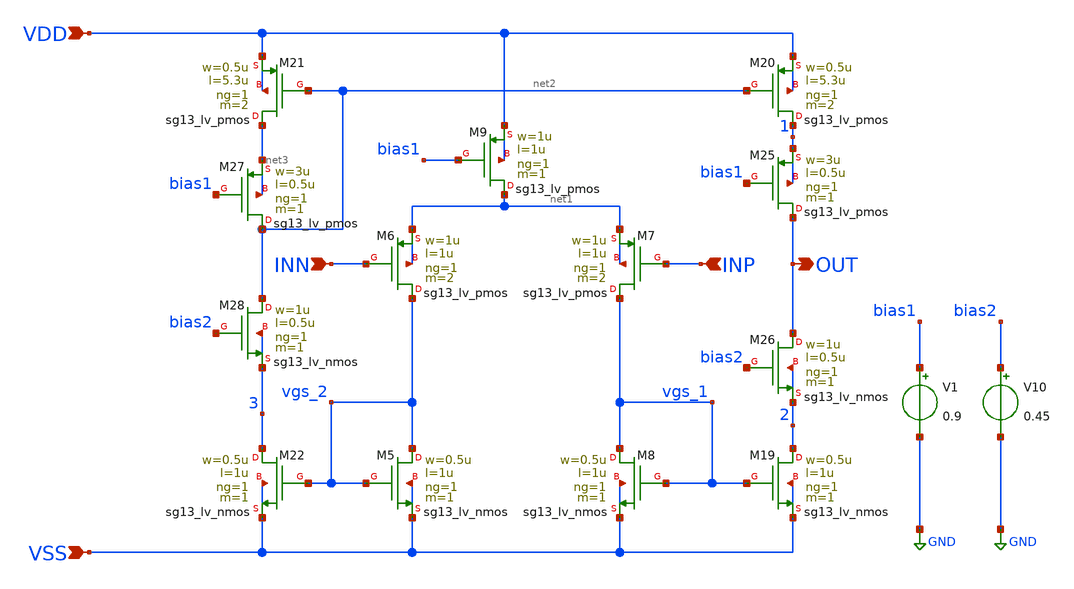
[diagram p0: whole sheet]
** sch_path: 10_xschem/ota.sch
**.subckt ota VDD VSS INN INP OUT
*.ipin VDD
*.ipin VSS
*.ipin INN
*.ipin INP
*.opin OUT
XM5 vgs_2 vgs_2 VSS VSS sg13_lv_nmos w=0.5u l=1u ng=1 m=1 mm_ok=1
XM6 vgs_2 INN net1 net1 sg13_lv_pmos w=1u l=1u ng=1 m=2 mm_ok=1
XM7 vgs_1 INP net1 net1 sg13_lv_pmos w=1u l=1u ng=1 m=2 mm_ok=1
XM8 vgs_1 vgs_1 VSS VSS sg13_lv_nmos w=0.5u l=1u ng=1 m=1 mm_ok=1
XM9 net1 bias1 VDD VDD sg13_lv_pmos w=1u l=1u ng=1 m=1 mm_ok=1
XM19 2 vgs_1 VSS VSS sg13_lv_nmos w=0.5u l=1u ng=1 m=1 mm_ok=1
XM20 1 net2 VDD VDD sg13_lv_pmos w=0.5u l=5.3u ng=1 m=2 mm_ok=1
XM21 net3 net2 VDD VDD sg13_lv_pmos w=0.5u l=5.3u ng=1 m=2 mm_ok=1
XM22 3 vgs_2 VSS VSS sg13_lv_nmos w=0.5u l=1u ng=1 m=1 mm_ok=1
V1 bias1 GND 0.9
XM25 OUT bias1 1 1 sg13_lv_pmos w=3u l=0.5u ng=1 m=1 mm_ok=1
XM26 OUT bias2 2 2 sg13_lv_nmos w=1u l=0.5u ng=1 m=1 mm_ok=1
XM27 net2 bias1 net3 net3 sg13_lv_pmos w=3u l=0.5u ng=1 m=1 mm_ok=1
XM28 net2 bias2 3 3 sg13_lv_nmos w=1u l=0.5u ng=1 m=1 mm_ok=1
V10 bias2 GND 0.45
**.ends
.GLOBAL GND
.end
